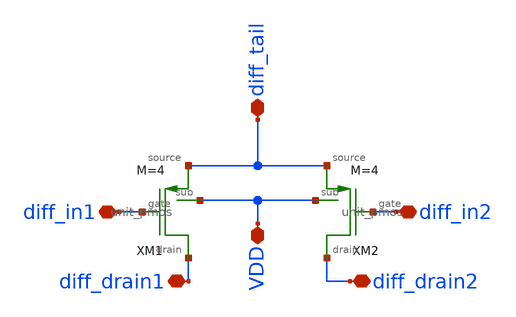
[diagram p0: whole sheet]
** sch_path: designs/libs/core_differential_pair/pmos_differential_pair/pmos_differential_pair.sch
**.subckt pmos_differential_pair diff_tail diff_drain1 diff_drain2 diff_in1 diff_in2 VDD
*.iopin diff_tail
*.iopin diff_drain1
*.iopin diff_drain2
*.iopin diff_in1
*.iopin diff_in2
*.iopin VDD
XM1 diff_drain1 VDD diff_in1 diff_tail unit_pmos M=4
XM2 diff_drain2 VDD diff_in2 diff_tail unit_pmos M=4
**.ends

* expanding   symbol:  libs/core_single_mos/unit_pmos/unit_pmos.sym # of pins=4
** sym_path: designs/libs/core_single_mos/unit_pmos/unit_pmos.sym
** sch_path: designs/libs/core_single_mos/unit_pmos/unit_pmos.sch
.subckt unit_pmos drain sub gate source
*.iopin drain
*.iopin source
*.iopin sub
*.iopin gate
**** begin user architecture code

.param M=1

**** end user architecture code
XM1 drain gate source sub pfet_03v3 L=0.5u W=48u nf=8 ad='int((nf+1)/2) * W/nf * 0.18u' as='int((nf+2)/2) * W/nf * 0.18u'
+ pd='2*int((nf+1)/2) * (W/nf + 0.18u)' ps='2*int((nf+2)/2) * (W/nf + 0.18u)' nrd='0.18u / W' nrs='0.18u / W'
+ sa=0 sb=0 sd=0 m={M}
.ends

.end
